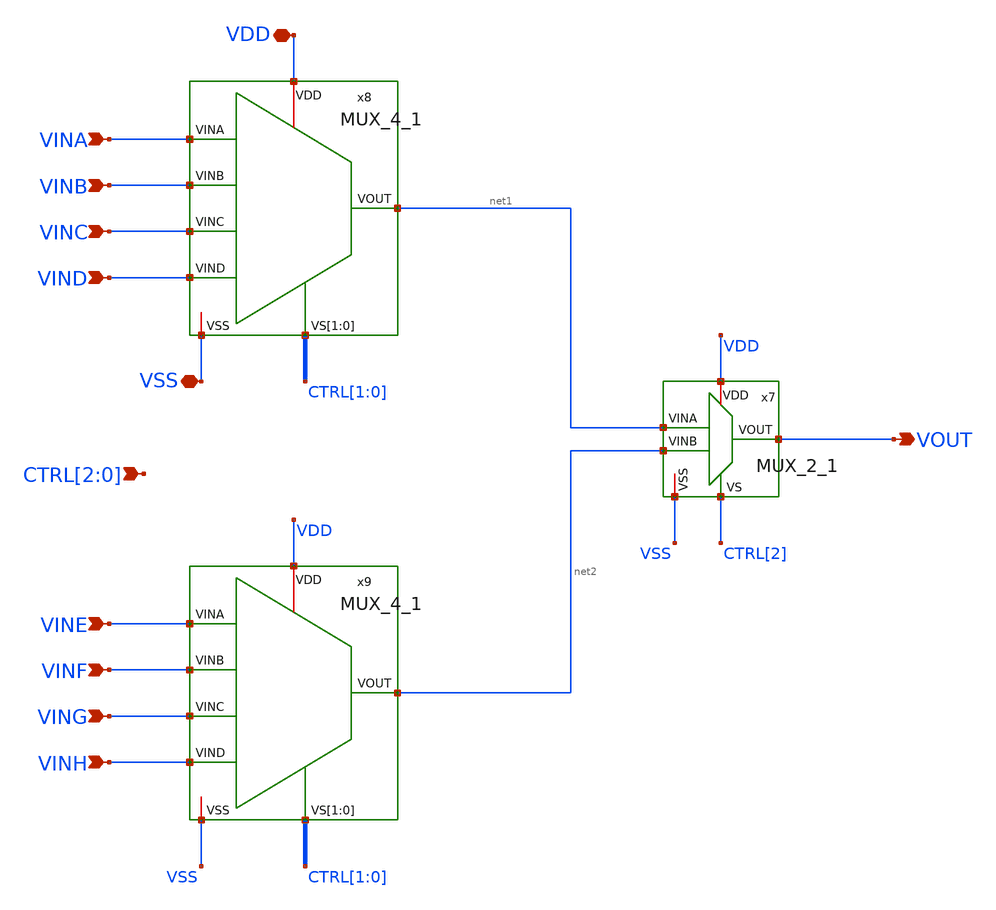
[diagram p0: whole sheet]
** sch_path: 27_03_26/TOP_MAXI/Esquematicos/MUX_8_1.sch
**.subckt MUX_8_1 VSS VOUT VDD VINA VINB VINC VIND CTRL[2],CTRL[1],CTRL[0] VINE VINF VING VINH
*.iopin VSS
*.opin VOUT
*.iopin VDD
*.ipin VINA
*.ipin VINB
*.ipin VINC
*.ipin VIND
*.ipin CTRL[2],CTRL[1],CTRL[0]
*.ipin VINE
*.ipin VINF
*.ipin VING
*.ipin VINH
x7 VDD net1 VOUT CTRL[2] net2 VSS MUX_2_1
x8 VINA VINB VDD net1 CTRL[1] CTRL[0] VINC VSS VIND MUX_4_1
x9 VINE VINF VDD net2 CTRL[1] CTRL[0] VING VSS VINH MUX_4_1
**.ends
.end
